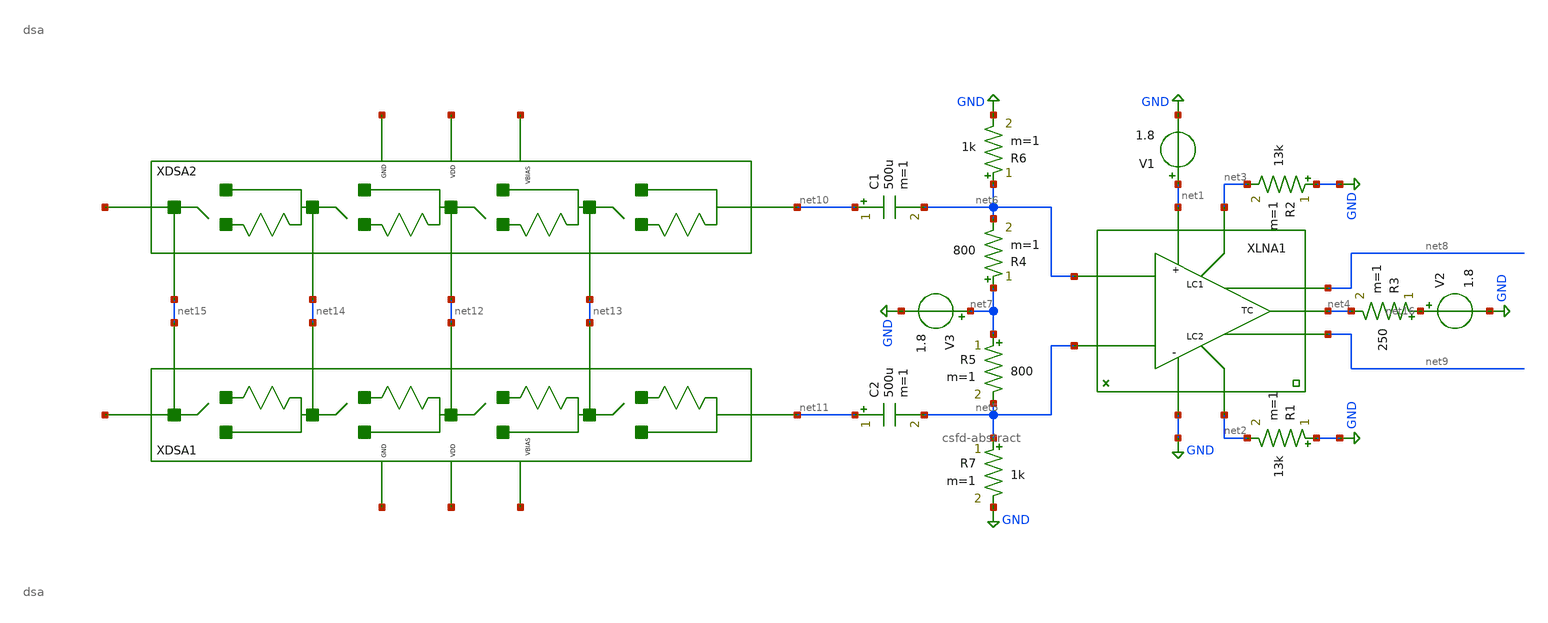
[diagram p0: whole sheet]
** sch_path: xschem/compiled.sch
**.subckt compiled
XLNA1 net6 net5 net1 GND net8 net9 net3 net4 net2 csfd-abstract
V1 net1 GND 1.8
R1 GND net2 13k m=1
R2 GND net3 13k m=1
R3 net16 net4 250 m=1
V2 net16 GND 1.8
V3 net7 GND 1.8
R4 net7 net6 800 m=1
R5 net7 net5 800 m=1
R6 net6 GND 1k m=1
R7 net5 GND 1k m=1
C1 net10 net6 500u m=1
C2 net11 net5 500u m=1
XDSA1 net17 net15 net14 net12 net13 net11 net18 net19 net20 dsa
XDSA2 net21 net15 net14 net12 net13 net10 net22 net23 net24 dsa
**.ends
.GLOBAL GND
.end
